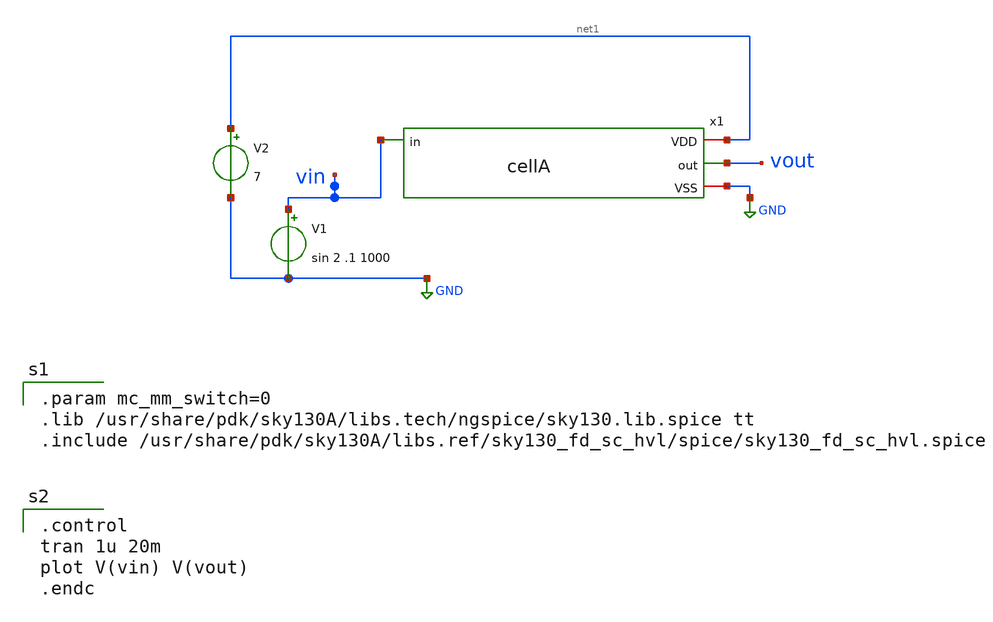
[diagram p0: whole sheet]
** sch_path: xschem/cellA_tb.sch
**.subckt cellA_tb
V1 vin GND sin 2 .1 1000
V2 net1 GND 7
x1 net1 vout vin GND cellA
**** begin user architecture code

.param mc_mm_switch=0
.lib /usr/share/pdk/sky130A/libs.tech/ngspice/sky130.lib.spice tt
.include /usr/share/pdk/sky130A/libs.ref/sky130_fd_sc_hvl/spice/sky130_fd_sc_hvl.spice


.control
tran 1u 20m
plot V(vin) V(vout)
.endc

**** end user architecture code
**.ends

* expanding   symbol:  cellA.sym # of pins=4
** sym_path: xschem/cellA.sym
** sch_path: xschem/cellA.sch
.subckt cellA VDD out in VSS
*.ipin in
*.iopin VDD
*.opin out
*.iopin VSS
XM3 out in VSS GND sky130_fd_pr__nfet_g5v0d10v5 L=0.8 W=2 nf=1 ad='int((nf+1)/2) * W/nf * 0.29' as='int((nf+2)/2) * W/nf * 0.29'
+ pd='2*int((nf+1)/2) * (W/nf + 0.29)' ps='2*int((nf+2)/2) * (W/nf + 0.29)' nrd='0.29 / W' nrs='0.29 / W'
+ sa=0 sb=0 sd=0 mult=1 m=1
XR1 out VDD GND sky130_fd_pr__res_high_po_0p35 L=20 mult=1 m=1
.ends

.GLOBAL GND
.end
